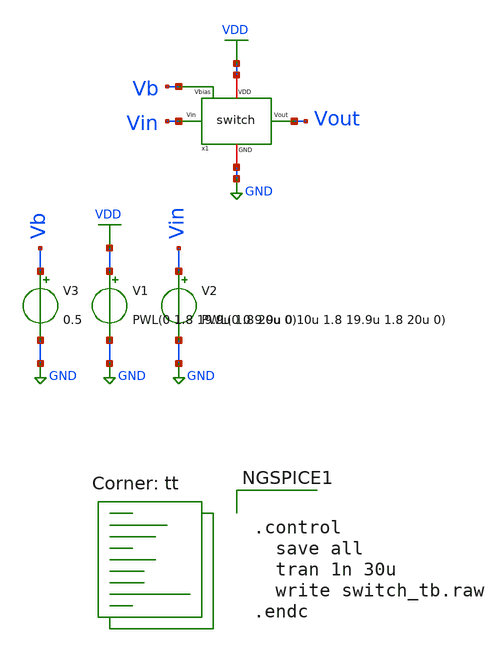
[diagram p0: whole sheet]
** sch_path: SNN/WU_Circuit_tb.sch
**.subckt WU_Circuit_tb
V1 VDD GND PWL(0 1.8 19.9u 1.8 20u 0)
V2 Vin GND PWL(0 0 9.9u 0 10u 1.8 19.9u 1.8 20u 0)
V3 Vb GND 0.5
x1 Vin GND VDD Vout Vb switch
**** begin user architecture code
.lib $::SKYWATER_MODELS/sky130.lib.spice tt


.control
  save all
  tran 1n 30u
  write switch_tb.raw
.endc


**** end user architecture code
**.ends

* expanding   symbol:  /home/ricardo/RATT_repos/Proyectos_xschem/switch/switch.sym # of pins=5
** sym_path: switch/switch.sym
** sch_path: switch/switch.sch
.subckt switch Vin GND VDD Vout Vbias
*.iopin GND
*.iopin VDD
*.opin Vout
*.ipin Vin
*.ipin Vbias
XM1 Vout net1 Vin VDD sky130_fd_pr__pfet_01v8 L=0.15 W=0.45 nf=1 ad='int((nf+1)/2) * W/nf * 0.29' as='int((nf+2)/2) * W/nf * 0.29'
+ pd='2*int((nf+1)/2) * (W/nf + 0.29)' ps='2*int((nf+2)/2) * (W/nf + 0.29)' nrd='0.29 / W' nrs='0.29 / W'
+ sa=0 sb=0 sd=0 mult=1 m=1
XM2 Vin Vin Vout GND sky130_fd_pr__nfet_01v8 L=0.15 W=0.45 nf=1 ad='int((nf+1)/2) * W/nf * 0.29' as='int((nf+2)/2) * W/nf * 0.29'
+ pd='2*int((nf+1)/2) * (W/nf + 0.29)' ps='2*int((nf+2)/2) * (W/nf + 0.29)' nrd='0.29 / W' nrs='0.29 / W'
+ sa=0 sb=0 sd=0 mult=1 m=1
XM3 net1 Vin VDD VDD sky130_fd_pr__pfet_01v8 L=0.15 W=0.45 nf=1 ad='int((nf+1)/2) * W/nf * 0.29' as='int((nf+2)/2) * W/nf * 0.29'
+ pd='2*int((nf+1)/2) * (W/nf + 0.29)' ps='2*int((nf+2)/2) * (W/nf + 0.29)' nrd='0.29 / W' nrs='0.29 / W'
+ sa=0 sb=0 sd=0 mult=1 m=1
XM4 net1 Vin GND GND sky130_fd_pr__nfet_01v8 L=0.15 W=0.45 nf=1 ad='int((nf+1)/2) * W/nf * 0.29' as='int((nf+2)/2) * W/nf * 0.29'
+ pd='2*int((nf+1)/2) * (W/nf + 0.29)' ps='2*int((nf+2)/2) * (W/nf + 0.29)' nrd='0.29 / W' nrs='0.29 / W'
+ sa=0 sb=0 sd=0 mult=1 m=1
XM5 Vout Vbias GND GND sky130_fd_pr__nfet_01v8 L=0.15 W=0.45 nf=1 ad='int((nf+1)/2) * W/nf * 0.29' as='int((nf+2)/2) * W/nf * 0.29'
+ pd='2*int((nf+1)/2) * (W/nf + 0.29)' ps='2*int((nf+2)/2) * (W/nf + 0.29)' nrd='0.29 / W' nrs='0.29 / W'
+ sa=0 sb=0 sd=0 mult=1 m=1
.ends

.GLOBAL GND
.GLOBAL VDD
.end
